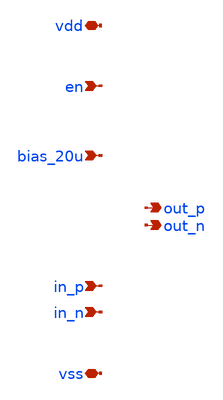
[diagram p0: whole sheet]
** sch_path: design/io_driver/io_driver_pex.sch
**.subckt io_driver_pex en bias_20u vss vdd out_p out_n in_n in_p
*.ipin en
*.ipin bias_20u
*.iopin vss
*.iopin vdd
*.opin out_p
*.opin out_n
*.ipin in_n
*.ipin in_p
**** begin user architecture code



* NGSPICE file created from io_driver.ext - technology: sky130A

.subckt sky130_fd_pr__res_xhigh_po_0p35_0-35_3-50 VSUBS a_n36_1150# a_n36_18#
X0 a_n36_18# a_n36_1150# VSUBS sky130_fd_pr__res_xhigh_po w=350000u l=3.5e+06u
C0 a_n36_18# VSUBS 0.35fF
C1 a_n36_1150# VSUBS 0.35fF
.ends

.subckt sky130_fd_pr__nfet_01v8_lvt_0-42_0-15 a_n73_n70# w_n99_n96# a_n33_36# a_15_n70#
X0 a_15_n70# a_n33_36# a_n73_n70# w_n99_n96# sky130_fd_pr__nfet_01v8_lvt ad=1.218e+11p pd=1.42e+06u
+ as=1.218e+11p ps=1.42e+06u w=420000u l=150000u
C0 a_15_n70# a_n33_36# 0.02fF
C1 a_15_n70# a_n73_n70# 0.15fF
C2 a_n33_36# a_n73_n70# 0.02fF
C3 a_15_n70# w_n99_n96# 0.03fF
C4 a_n73_n70# w_n99_n96# 0.03fF
C5 a_n33_36# w_n99_n96# 0.12fF
.ends

.subckt sky130_fd_sc_hs__inv_1 VGND Y VPWR A VPB VNB
X0 Y A VPWR VPB sky130_fd_pr__pfet_01v8 ad=3.304e+11p pd=2.83e+06u as=3.864e+11p ps=2.93e+06u
+ w=1.12e+06u l=150000u
X1 Y A VGND VNB sky130_fd_pr__nfet_01v8_lvt ad=2.109e+11p pd=2.05e+06u as=2.627e+11p ps=2.19e+06u
+ w=740000u l=150000u
C0 VGND VPWR 0.01fF
C1 Y VGND 0.19fF
C2 VPWR VPB 0.02fF
C3 VPWR A 0.08fF
C4 Y A 0.26fF
C5 VGND A 0.08fF
C6 Y VPWR 0.24fF
C7 VGND VNB 0.37fF
C8 Y VNB 0.19fF
C9 VPWR VNB 0.36fF
C10 A VNB 0.36fF
C11 VPB VNB 0.41fF
.ends

.subckt sky130_fd_pr__cap_mim_m3_1_20-00_20-00 VSUBS c1_100_100# m3_0_0#
X0 c1_100_100# m3_0_0# sky130_fd_pr__cap_mim_m3_1 l=2e+07u w=2e+07u
C0 m3_0_0# c1_100_100# 39.78fF
C1 m3_0_0# VSUBS 8.90fF
.ends

.subckt sky130_fd_pr__nfet_01v8_lvt_1-00_0-15_nf2 w_n151_n126# a_n33_n100# a_63_n100#  a_n81_n188#
+ a_n125_n100# a_15_122#
X0 a_n33_n100# a_n81_n188# a_n125_n100# w_n151_n126# sky130_fd_pr__nfet_01v8_lvt ad=3.3e+11p
+ pd=2.66e+06u as=3.1e+11p ps=2.62e+06u w=1e+06u l=150000u
X1 a_63_n100# a_15_122# a_n33_n100# w_n151_n126# sky130_fd_pr__nfet_01v8_lvt ad=3.1e+11p
+ pd=2.62e+06u as=0p ps=0u w=1e+06u l=150000u
C0 a_63_n100# a_n125_n100# 0.11fF
C1 a_n33_n100# a_63_n100# 0.29fF
C2 a_15_122# a_n81_n188# 0.02fF
C3 a_n33_n100# a_n125_n100# 0.29fF
C4 a_63_n100# w_n151_n126# 0.03fF
C5 a_n33_n100# w_n151_n126# 0.03fF
C6 a_n125_n100# w_n151_n126# 0.03fF
C7 a_n81_n188# w_n151_n126# 0.12fF
C8 a_15_122# w_n151_n126# 0.12fF
.ends

.subckt sky130_fd_pr__nfet_01v8_lvt_5-00_0-15_nf10 a_716_1110# w_n26_62# a_236_0#  a_188_88#
+ a_572_88# a_620_0# a_92_88# a_908_1110# a_140_1110# a_284_88# a_956_88#  a_428_0# a_812_0# a_380_88#
+ a_332_1110# a_668_88# a_0_88# a_524_1110# a_764_88#  a_44_0# a_476_88# a_860_88#
X0 a_92_88# a_44_0# a_0_88# w_n26_62# sky130_fd_pr__nfet_01v8_lvt ad=1.65e+12p pd=1.066e+07u
+ as=1.55e+12p ps=1.062e+07u w=5e+06u l=150000u
X1 a_188_88# a_140_1110# a_92_88# w_n26_62# sky130_fd_pr__nfet_01v8_lvt ad=1.65e+12p pd=1.066e+07u
+ as=0p ps=0u w=5e+06u l=150000u
X2 a_764_88# a_716_1110# a_668_88# w_n26_62# sky130_fd_pr__nfet_01v8_lvt ad=1.65e+12p pd=1.066e+07u
+ as=1.65e+12p ps=1.066e+07u w=5e+06u l=150000u
X3 a_284_88# a_236_0# a_188_88# w_n26_62# sky130_fd_pr__nfet_01v8_lvt ad=1.65e+12p pd=1.066e+07u
+ as=0p ps=0u w=5e+06u l=150000u
X4 a_956_88# a_908_1110# a_860_88# w_n26_62# sky130_fd_pr__nfet_01v8_lvt ad=1.55e+12p pd=1.062e+07u
+ as=1.65e+12p ps=1.066e+07u w=5e+06u l=150000u
X5 a_860_88# a_812_0# a_764_88# w_n26_62# sky130_fd_pr__nfet_01v8_lvt ad=0p pd=0u as=0p ps=0u
+ w=5e+06u l=150000u
X6 a_476_88# a_428_0# a_380_88# w_n26_62# sky130_fd_pr__nfet_01v8_lvt ad=1.65e+12p pd=1.066e+07u
+ as=1.65e+12p ps=1.066e+07u w=5e+06u l=150000u
X7 a_380_88# a_332_1110# a_284_88# w_n26_62# sky130_fd_pr__nfet_01v8_lvt ad=0p pd=0u as=0p ps=0u
+ w=5e+06u l=150000u
X8 a_668_88# a_620_0# a_572_88# w_n26_62# sky130_fd_pr__nfet_01v8_lvt ad=0p pd=0u as=1.65e+12p
+ ps=1.066e+07u w=5e+06u l=150000u
X9 a_572_88# a_524_1110# a_476_88# w_n26_62# sky130_fd_pr__nfet_01v8_lvt ad=0p pd=0u as=0p ps=0u
+ w=5e+06u l=150000u
C0 a_380_88# a_0_88# 0.23fF
C1 a_668_88# a_380_88# 0.32fF
C2 a_668_88# a_956_88# 0.32fF
C3 a_572_88# a_188_88# 0.23fF
C4 a_476_88# a_284_88# 0.52fF
C5 a_428_0# a_812_0# 0.02fF
C6 a_428_0# a_620_0# 0.04fF
C7 a_908_1110# a_812_0# 0.02fF
C8 a_428_0# a_332_1110# 0.02fF
C9 a_620_0# a_524_1110# 0.02fF
C10 a_428_0# a_236_0# 0.04fF
C11 a_524_1110# a_332_1110# 0.04fF
C12 a_764_88# a_380_88# 0.23fF
C13 a_716_1110# a_908_1110# 0.04fF
C14 a_764_88# a_956_88# 0.52fF
C15 a_572_88# a_284_88# 0.32fF
C16 a_668_88# a_764_88# 1.44fF
C17 a_716_1110# a_524_1110# 0.04fF
C18 a_380_88# a_476_88# 1.44fF
C19 a_860_88# a_956_88# 1.44fF
C20 a_332_1110# a_140_1110# 0.04fF
C21 a_668_88# a_860_88# 0.52fF
C22 a_668_88# a_476_88# 0.52fF
C23 a_236_0# a_140_1110# 0.02fF
C24 a_428_0# a_524_1110# 0.02fF
C25 a_380_88# a_572_88# 0.52fF
C26 a_572_88# a_956_88# 0.23fF
C27 a_524_1110# a_908_1110# 0.02fF
C28 a_764_88# a_860_88# 1.44fF
C29 a_668_88# a_572_88# 1.44fF
C30 a_764_88# a_476_88# 0.32fF
C31 a_236_0# a_44_0# 0.04fF
C32 a_92_88# a_188_88# 1.44fF
C33 a_764_88# a_572_88# 0.52fF
C34 a_860_88# a_476_88# 0.23fF
C35 a_524_1110# a_140_1110# 0.02fF
C36 a_92_88# a_284_88# 0.52fF
C37 a_428_0# a_44_0# 0.02fF
C38 a_860_88# a_572_88# 0.32fF
C39 a_476_88# a_572_88# 1.44fF
C40 a_188_88# a_284_88# 1.44fF
C41 a_0_88# a_92_88# 1.44fF
C42 a_380_88# a_92_88# 0.32fF
C43 a_140_1110# a_44_0# 0.02fF
C44 a_0_88# a_188_88# 0.52fF
C45 a_380_88# a_188_88# 0.52fF
C46 a_0_88# a_284_88# 0.32fF
C47 a_620_0# a_812_0# 0.04fF
C48 a_380_88# a_284_88# 1.44fF
C49 a_668_88# a_284_88# 0.23fF
C50 a_476_88# a_92_88# 0.23fF
C51 a_620_0# a_236_0# 0.02fF
C52 a_716_1110# a_812_0# 0.02fF
C53 a_716_1110# a_620_0# 0.02fF
C54 a_236_0# a_332_1110# 0.02fF
C55 a_716_1110# a_332_1110# 0.02fF
C56 a_476_88# a_188_88# 0.32fF
C57 a_956_88# w_n26_62# 0.03fF
C58 a_860_88# w_n26_62# 0.03fF
C59 a_764_88# w_n26_62# 0.03fF
C60 a_668_88# w_n26_62# 0.03fF
C61 a_572_88# w_n26_62# 0.03fF
C62 a_476_88# w_n26_62# 0.03fF
C63 a_380_88# w_n26_62# 0.03fF
C64 a_284_88# w_n26_62# 0.03fF
C65 a_188_88# w_n26_62# 0.03fF
C66 a_92_88# w_n26_62# 0.03fF
C67 a_0_88# w_n26_62# 0.03fF
C68 a_812_0# w_n26_62# 0.12fF
C69 a_908_1110# w_n26_62# 0.12fF
C70 a_620_0# w_n26_62# 0.12fF
C71 a_716_1110# w_n26_62# 0.12fF
C72 a_428_0# w_n26_62# 0.12fF
C73 a_524_1110# w_n26_62# 0.12fF
C74 a_236_0# w_n26_62# 0.12fF
C75 a_332_1110# w_n26_62# 0.12fF
C76 a_44_0# w_n26_62# 0.12fF
C77 a_140_1110# w_n26_62# 0.12fF
.ends

*.subckt io_driver bias_20u vdd en in_n in_p vss out_n out_p
Xsky130_fd_pr__res_xhigh_po_0p35_0-35_3-50_0 vss m3_535_2996# m1_3156_3760#
+ sky130_fd_pr__res_xhigh_po_0p35_0-35_3-50
Xsky130_fd_pr__res_xhigh_po_0p35_0-35_3-50_1 vss m4_3735_2549# m1_3156_3760#
+ sky130_fd_pr__res_xhigh_po_0p35_0-35_3-50
Xsky130_fd_pr__nfet_01v8_lvt_0-42_0-15_0 m1_3156_3760# vss sky130_fd_sc_hs__inv_1_1/Y  vss
+ sky130_fd_pr__nfet_01v8_lvt_0-42_0-15
Xsky130_fd_sc_hs__inv_1_0 vss sky130_fd_sc_hs__inv_1_0/Y vdd sky130_fd_sc_hs__inv_1_1/Y  vdd vss
+ sky130_fd_sc_hs__inv_1
Xsky130_fd_sc_hs__inv_1_1 vss sky130_fd_sc_hs__inv_1_1/Y vdd en vdd vss sky130_fd_sc_hs__inv_1
Xsky130_fd_pr__cap_mim_m3_1_20-00_20-00_0 vss in_p m3_535_2996#
+ sky130_fd_pr__cap_mim_m3_1_20-00_20-00
Xsky130_fd_pr__cap_mim_m3_1_20-00_20-00_1 vss in_n m4_3735_2549#
+ sky130_fd_pr__cap_mim_m3_1_20-00_20-00
Xsky130_fd_pr__nfet_01v8_lvt_1-00_0-15_nf2_0 vss m1_3156_3760# vss sky130_fd_sc_hs__inv_1_0/Y
+  bias_20u m1_3156_3760# sky130_fd_pr__nfet_01v8_lvt_1-00_0-15_nf2
Xsky130_fd_pr__nfet_01v8_lvt_5-00_0-15_nf10_0[0|0] m3_535_2996# vss m3_535_2996# vss  vss
+ m3_535_2996# out_p m3_535_2996# m3_535_2996# out_p vss m3_535_2996# m3_535_2996#  vss m3_535_2996# out_p vss
+ m3_535_2996# vss m3_535_2996# out_p out_p sky130_fd_pr__nfet_01v8_lvt_5-00_0-15_nf10
Xsky130_fd_pr__nfet_01v8_lvt_5-00_0-15_nf10_0[1|0] m3_535_2996# vss m3_535_2996# vss  vss
+ m3_535_2996# out_p m3_535_2996# m3_535_2996# out_p vss m3_535_2996# m3_535_2996#  vss m3_535_2996# out_p vss
+ m3_535_2996# vss m3_535_2996# out_p out_p sky130_fd_pr__nfet_01v8_lvt_5-00_0-15_nf10
Xsky130_fd_pr__nfet_01v8_lvt_5-00_0-15_nf10_0[0|1] m3_535_2996# vss m3_535_2996# vss  vss
+ m3_535_2996# out_p m3_535_2996# m3_535_2996# out_p vss m3_535_2996# m3_535_2996#  vss m3_535_2996# out_p vss
+ m3_535_2996# vss m3_535_2996# out_p out_p sky130_fd_pr__nfet_01v8_lvt_5-00_0-15_nf10
Xsky130_fd_pr__nfet_01v8_lvt_5-00_0-15_nf10_0[1|1] m3_535_2996# vss m3_535_2996# vss  vss
+ m3_535_2996# out_p m3_535_2996# m3_535_2996# out_p vss m3_535_2996# m3_535_2996#  vss m3_535_2996# out_p vss
+ m3_535_2996# vss m3_535_2996# out_p out_p sky130_fd_pr__nfet_01v8_lvt_5-00_0-15_nf10
Xsky130_fd_pr__nfet_01v8_lvt_5-00_0-15_nf10_1[0|0] m4_3735_2549# vss m4_3735_2549#  vss vss
+ m4_3735_2549# out_n m4_3735_2549# m4_3735_2549# out_n vss m4_3735_2549#  m4_3735_2549# vss m4_3735_2549# out_n
+ vss m4_3735_2549# vss m4_3735_2549# out_n  out_n sky130_fd_pr__nfet_01v8_lvt_5-00_0-15_nf10
Xsky130_fd_pr__nfet_01v8_lvt_5-00_0-15_nf10_1[1|0] m4_3735_2549# vss m4_3735_2549#  vss vss
+ m4_3735_2549# out_n m4_3735_2549# m4_3735_2549# out_n vss m4_3735_2549#  m4_3735_2549# vss m4_3735_2549# out_n
+ vss m4_3735_2549# vss m4_3735_2549# out_n  out_n sky130_fd_pr__nfet_01v8_lvt_5-00_0-15_nf10
Xsky130_fd_pr__nfet_01v8_lvt_5-00_0-15_nf10_1[0|1] m4_3735_2549# vss m4_3735_2549#  vss vss
+ m4_3735_2549# out_n m4_3735_2549# m4_3735_2549# out_n vss m4_3735_2549#  m4_3735_2549# vss m4_3735_2549# out_n
+ vss m4_3735_2549# vss m4_3735_2549# out_n  out_n sky130_fd_pr__nfet_01v8_lvt_5-00_0-15_nf10
Xsky130_fd_pr__nfet_01v8_lvt_5-00_0-15_nf10_1[1|1] m4_3735_2549# vss m4_3735_2549#  vss vss
+ m4_3735_2549# out_n m4_3735_2549# m4_3735_2549# out_n vss m4_3735_2549#  m4_3735_2549# vss m4_3735_2549# out_n
+ vss m4_3735_2549# vss m4_3735_2549# out_n  out_n sky130_fd_pr__nfet_01v8_lvt_5-00_0-15_nf10
C0 sky130_fd_sc_hs__inv_1_0/Y vdd 0.15fF
C1 out_n m4_3735_2549# 7.77fF
C2 sky130_fd_sc_hs__inv_1_1/Y sky130_fd_sc_hs__inv_1_0/Y 6.22fF
C3 m1_3156_3760# m3_535_2996# 0.27fF
C4 m1_3156_3760# sky130_fd_sc_hs__inv_1_1/Y 0.11fF
C5 sky130_fd_sc_hs__inv_1_1/Y vdd 0.11fF
C6 m1_3156_3760# out_p 0.04fF
C7 sky130_fd_sc_hs__inv_1_0/Y m4_3735_2549# 0.16fF
C8 m1_3156_3760# m4_3735_2549# 0.15fF
C9 bias_20u sky130_fd_sc_hs__inv_1_0/Y 2.79fF
C10 sky130_fd_sc_hs__inv_1_0/Y en 0.02fF
C11 en vdd 0.02fF
C12 m3_535_2996# out_p 7.78fF
C13 m1_3156_3760# out_n 0.03fF
C14 m3_535_2996# m4_3735_2549# 0.19fF
C15 sky130_fd_sc_hs__inv_1_1/Y m4_3735_2549# 0.47fF
C16 bias_20u m3_535_2996# 0.09fF
C17 sky130_fd_sc_hs__inv_1_1/Y bias_20u 1.37fF
C18 sky130_fd_sc_hs__inv_1_1/Y en 0.22fF
C19 bias_20u m4_3735_2549# 0.09fF
C20 out_n vss 12.88fF
C21 out_p vss 12.57fF
C22 bias_20u vss 12.83fF
C23 in_n vss 0.22fF
C24 m4_3735_2549# vss 17.83fF
C25 in_p vss 0.01fF
C26 m3_535_2996# vss 13.26fF
C27 vdd vss 2.30fF
C28 en vss 0.50fF
C29 sky130_fd_sc_hs__inv_1_0/Y vss 2.99fF
C30 sky130_fd_sc_hs__inv_1_1/Y vss 2.49fF
C31 m1_3156_3760# vss 0.07fF
*.ends




**** end user architecture code
**.ends
.end
